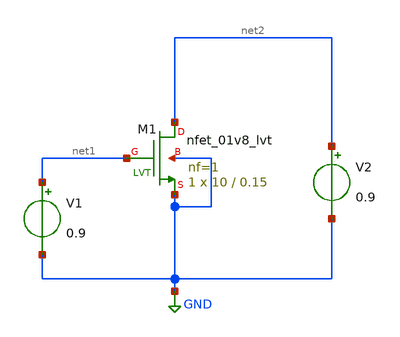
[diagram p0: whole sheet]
** sch_path: MOS-Design-Parameters/NMOS/act6.sch
**.subckt act6
XM1 net2 net1 GND GND sky130_fd_pr__nfet_01v8_lvt L=0.15 W=10 nf=1 ad='int((nf+1)/2) * W/nf * 0.29' as='int((nf+2)/2) * W/nf * 0.29'
+ pd='2*int((nf+1)/2) * (W/nf + 0.29)' ps='2*int((nf+2)/2) * (W/nf + 0.29)' nrd='0.29 / W' nrs='0.29 / W'
+ sa=0 sb=0 sd=0 mult=1 m=1
V1 net1 GND 0.9
V2 net2 GND 0.9
**** begin user architecture code


.lib /usr/local/share/pdk/sky130A/libs.tech/ngspice/sky130.lib.spice ff
.option wnflag=1 scale=1e-6

.control
save all

save @m.xm1.msky130_fd_pr__nfet_01v8_lvt[id]
save @m.xm1.msky130_fd_pr__nfet_01v8_lvt[gm]
save @m.xm1.msky130_fd_pr__nfet_01v8_lvt[cgs]
save @m.xm1.msky130_fd_pr__nfet_01v8_lvt[cgd]

dc v1 0 1.8 1m

let id = @m.xm1.msky130_fd_pr__nfet_01v8_lvt[id]
let gm = @m.xm1.msky130_fd_pr__nfet_01v8_lvt[gm]
let cgs = @m.xm1.msky130_fd_pr__nfet_01v8_lvt[cgs]
let cgd = @m.xm1.msky130_fd_pr__nfet_01v8_lvt[cgd]

let gmoverid = gm/id
let vstar = 2/gmoverid
let cgg = cgs+cgd
let ft = gm/(2*pi*cgg)

*wrdata gmoverid-ff.txt gmoverid
wrdata vstar-ff.txt vstar
*wrdata ft-ff.txt ft

.endc


**** end user architecture code
**.ends
.GLOBAL GND
.end
